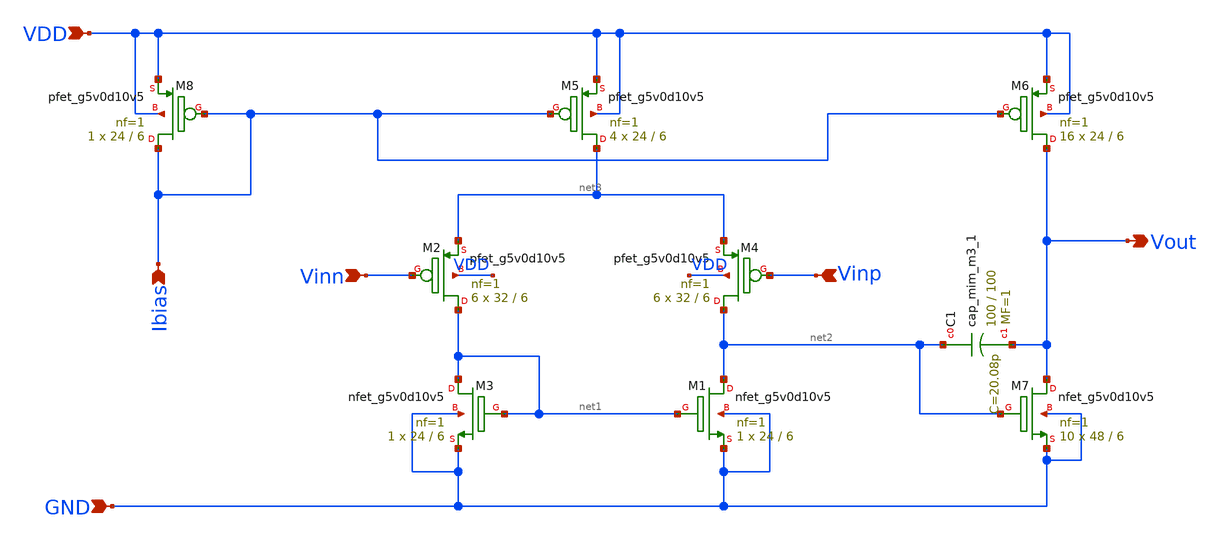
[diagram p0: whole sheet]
** sch_path: xschem/OpAmp_v0/OpAmp.sch
**.subckt OpAmp Vinn Vinp GND VDD Ibias Vout
*.ipin Vinn
*.ipin Vinp
*.ipin GND
*.ipin VDD
*.ipin Ibias
*.opin Vout
XM3 net1 net1 GND GND sky130_fd_pr__nfet_g5v0d10v5 L=6 W=24 nf=1 ad='int((nf+1)/2) * W/nf * 0.29' as='int((nf+2)/2) * W/nf * 0.29'
+ pd='2*int((nf+1)/2) * (W/nf + 0.29)' ps='2*int((nf+2)/2) * (W/nf + 0.29)' nrd='0.29 / W' nrs='0.29 / W'
+ sa=0 sb=0 sd=0 mult=1 m=1
XM1 net2 net1 GND GND sky130_fd_pr__nfet_g5v0d10v5 L=6 W=24 nf=1 ad='int((nf+1)/2) * W/nf * 0.29' as='int((nf+2)/2) * W/nf * 0.29'
+ pd='2*int((nf+1)/2) * (W/nf + 0.29)' ps='2*int((nf+2)/2) * (W/nf + 0.29)' nrd='0.29 / W' nrs='0.29 / W'
+ sa=0 sb=0 sd=0 mult=1 m=1
XM2 net1 Vinn net3 VDD sky130_fd_pr__pfet_g5v0d10v5 L=6 W=32 nf=1 ad='int((nf+1)/2) * W/nf * 0.29' as='int((nf+2)/2) * W/nf * 0.29'
+ pd='2*int((nf+1)/2) * (W/nf + 0.29)' ps='2*int((nf+2)/2) * (W/nf + 0.29)' nrd='0.29 / W' nrs='0.29 / W'
+ sa=0 sb=0 sd=0 mult=6 m=6
XM4 net2 Vinp net3 VDD sky130_fd_pr__pfet_g5v0d10v5 L=6 W=32 nf=1 ad='int((nf+1)/2) * W/nf * 0.29' as='int((nf+2)/2) * W/nf * 0.29'
+ pd='2*int((nf+1)/2) * (W/nf + 0.29)' ps='2*int((nf+2)/2) * (W/nf + 0.29)' nrd='0.29 / W' nrs='0.29 / W'
+ sa=0 sb=0 sd=0 mult=6 m=6
XM5 net3 Ibias VDD VDD sky130_fd_pr__pfet_g5v0d10v5 L=6 W=24 nf=1 ad='int((nf+1)/2) * W/nf * 0.29' as='int((nf+2)/2) * W/nf * 0.29'
+ pd='2*int((nf+1)/2) * (W/nf + 0.29)' ps='2*int((nf+2)/2) * (W/nf + 0.29)' nrd='0.29 / W' nrs='0.29 / W'
+ sa=0 sb=0 sd=0 mult=4 m=4
XM6 Vout Ibias VDD VDD sky130_fd_pr__pfet_g5v0d10v5 L=6 W=24 nf=1 ad='int((nf+1)/2) * W/nf * 0.29' as='int((nf+2)/2) * W/nf * 0.29'
+ pd='2*int((nf+1)/2) * (W/nf + 0.29)' ps='2*int((nf+2)/2) * (W/nf + 0.29)' nrd='0.29 / W' nrs='0.29 / W'
+ sa=0 sb=0 sd=0 mult=16 m=16
XM7 Vout net2 GND GND sky130_fd_pr__nfet_g5v0d10v5 L=6 W=48 nf=1 ad='int((nf+1)/2) * W/nf * 0.29' as='int((nf+2)/2) * W/nf * 0.29'
+ pd='2*int((nf+1)/2) * (W/nf + 0.29)' ps='2*int((nf+2)/2) * (W/nf + 0.29)' nrd='0.29 / W' nrs='0.29 / W'
+ sa=0 sb=0 sd=0 mult=10 m=10
XM8 Ibias Ibias VDD VDD sky130_fd_pr__pfet_g5v0d10v5 L=6 W=24 nf=1 ad='int((nf+1)/2) * W/nf * 0.29' as='int((nf+2)/2) * W/nf * 0.29'
+ pd='2*int((nf+1)/2) * (W/nf + 0.29)' ps='2*int((nf+2)/2) * (W/nf + 0.29)' nrd='0.29 / W' nrs='0.29 / W'
+ sa=0 sb=0 sd=0 mult=1 m=1
XC1 net2 Vout sky130_fd_pr__cap_mim_m3_1 W=100 L=100 MF=1 m=1
**.ends
.end
